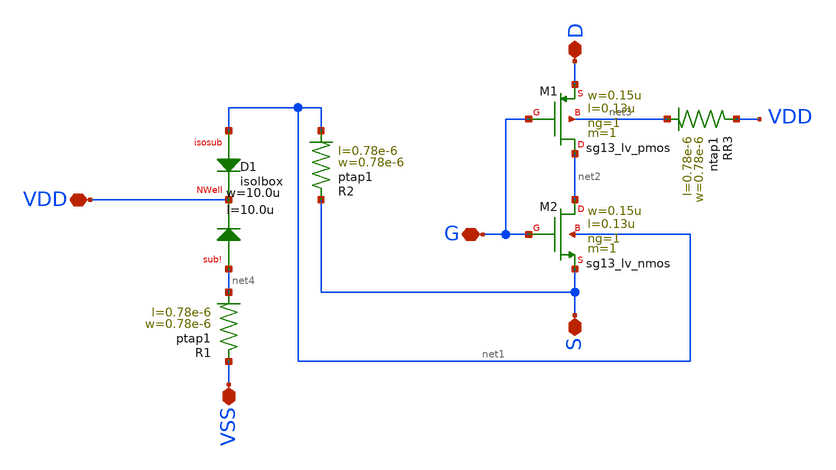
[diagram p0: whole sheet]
** sch_path: ihp-sg13g2/schematic/xschem/sg13_dnwell_inv.sch
**.subckt sg13_dnwell_inv VSS S VDD G D
*.iopin VSS
*.iopin S
*.iopin VDD
*.iopin G
*.iopin D
XD1 net1 VDD net4 isolbox l=10.0u w=10.0u
XM1 net2 G D net3 sg13_lv_pmos w=0.15u l=0.13u ng=1 m=1 mm_ok=1
XM2 net2 G S net1 sg13_lv_nmos w=0.15u l=0.13u ng=1 m=1 mm_ok=1
XR1 VSS net4 ptap1 R=262.8 w=0.78e-6 l=0.78e-6
XR2 S net1 ptap1 R=262.8 w=0.78e-6 l=0.78e-6
XR3 VDD net3 ntap1 R=262.8 w=0.78e-6 l=0.78e-6
**.ends
.end
